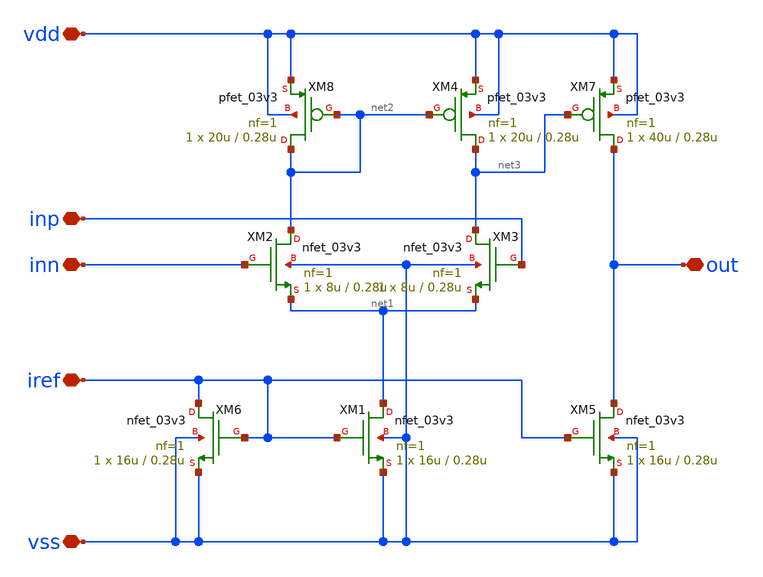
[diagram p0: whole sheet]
** sch_path: designs/libs/qw_core_analog_pkedit/NMOScomparator.sch
**.subckt NMOScomparator inp inn out vdd vss iref
*.iopin inp
*.iopin inn
*.iopin out
*.iopin vdd
*.iopin vss
*.iopin iref
XM6 iref iref vss vss nfet_03v3 L=0.28u W=16u nf=1 ad='int((nf+1)/2) * W/nf * 0.18u' as='int((nf+2)/2) * W/nf * 0.18u'
+ pd='2*int((nf+1)/2) * (W/nf + 0.18u)' ps='2*int((nf+2)/2) * (W/nf + 0.18u)' nrd='0.18u / W' nrs='0.18u / W'
+ sa=0 sb=0 sd=0 m=1
XM8 net2 net2 vdd vdd pfet_03v3 L=0.28u W=20u nf=1 ad='int((nf+1)/2) * W/nf * 0.18u' as='int((nf+2)/2) * W/nf * 0.18u'
+ pd='2*int((nf+1)/2) * (W/nf + 0.18u)' ps='2*int((nf+2)/2) * (W/nf + 0.18u)' nrd='0.18u / W' nrs='0.18u / W'
+ sa=0 sb=0 sd=0 m=1
XM1 net1 iref vss vss nfet_03v3 L=0.28u W=16u nf=1 ad='int((nf+1)/2) * W/nf * 0.18u' as='int((nf+2)/2) * W/nf * 0.18u'
+ pd='2*int((nf+1)/2) * (W/nf + 0.18u)' ps='2*int((nf+2)/2) * (W/nf + 0.18u)' nrd='0.18u / W' nrs='0.18u / W'
+ sa=0 sb=0 sd=0 m=1
XM2 net2 inn net1 vss nfet_03v3 L=0.28u W=8u nf=1 ad='int((nf+1)/2) * W/nf * 0.18u' as='int((nf+2)/2) * W/nf * 0.18u'
+ pd='2*int((nf+1)/2) * (W/nf + 0.18u)' ps='2*int((nf+2)/2) * (W/nf + 0.18u)' nrd='0.18u / W' nrs='0.18u / W'
+ sa=0 sb=0 sd=0 m=1
XM3 net3 inp net1 vss nfet_03v3 L=0.28u W=8u nf=1 ad='int((nf+1)/2) * W/nf * 0.18u' as='int((nf+2)/2) * W/nf * 0.18u'
+ pd='2*int((nf+1)/2) * (W/nf + 0.18u)' ps='2*int((nf+2)/2) * (W/nf + 0.18u)' nrd='0.18u / W' nrs='0.18u / W'
+ sa=0 sb=0 sd=0 m=1
XM4 net3 net2 vdd vdd pfet_03v3 L=0.28u W=20u nf=1 ad='int((nf+1)/2) * W/nf * 0.18u' as='int((nf+2)/2) * W/nf * 0.18u'
+ pd='2*int((nf+1)/2) * (W/nf + 0.18u)' ps='2*int((nf+2)/2) * (W/nf + 0.18u)' nrd='0.18u / W' nrs='0.18u / W'
+ sa=0 sb=0 sd=0 m=1
XM5 out iref vss vss nfet_03v3 L=0.28u W=16u nf=1 ad='int((nf+1)/2) * W/nf * 0.18u' as='int((nf+2)/2) * W/nf * 0.18u'
+ pd='2*int((nf+1)/2) * (W/nf + 0.18u)' ps='2*int((nf+2)/2) * (W/nf + 0.18u)' nrd='0.18u / W' nrs='0.18u / W'
+ sa=0 sb=0 sd=0 m=1
XM7 out net3 vdd vdd pfet_03v3 L=0.28u W=40u nf=1 ad='int((nf+1)/2) * W/nf * 0.18u' as='int((nf+2)/2) * W/nf * 0.18u'
+ pd='2*int((nf+1)/2) * (W/nf + 0.18u)' ps='2*int((nf+2)/2) * (W/nf + 0.18u)' nrd='0.18u / W' nrs='0.18u / W'
+ sa=0 sb=0 sd=0 m=1
**.ends
.end
